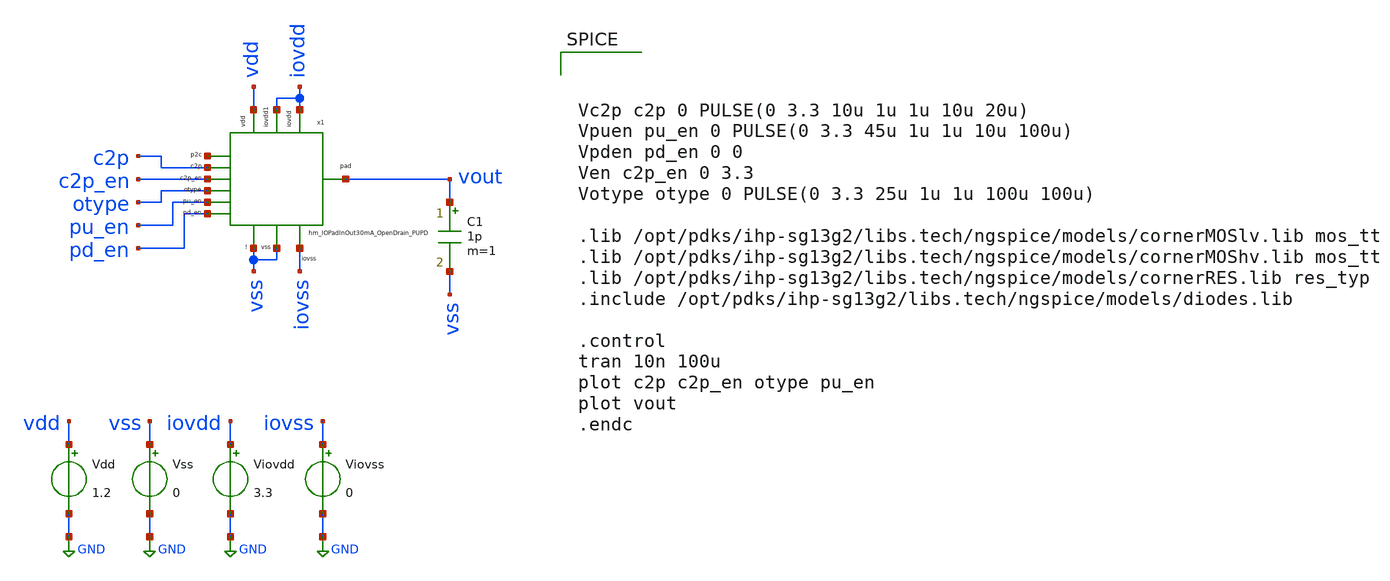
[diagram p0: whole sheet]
** sch_path: libs.tech/xschem/tests/test_hm_IOPadInOut30mA_OpenDrain_PUPD.sch
**.subckt test_hm_IOPadInOut30mA_OpenDrain_PUPD
Vdd vdd GND 1.2
Vss vss GND 0
Viovdd iovdd GND 3.3
Viovss iovss GND 0
x1 iovdd iovdd vdd pu_en c2p vout c2p_en pd_en otype net1 vss vss iovss
+ hm_IOPadInOut30mA_OpenDrain_PUPD
C1 vout vss 1p m=1
**** begin user architecture code



Vc2p c2p 0 PULSE(0 3.3 10u 1u 1u 10u 20u)
Vpuen pu_en 0 PULSE(0 3.3 45u 1u 1u 10u 100u)
Vpden pd_en 0 0
Ven c2p_en 0 3.3
Votype otype 0 PULSE(0 3.3 25u 1u 1u 100u 100u)

.lib /opt/pdks/ihp-sg13g2/libs.tech/ngspice/models/cornerMOSlv.lib mos_tt
.lib /opt/pdks/ihp-sg13g2/libs.tech/ngspice/models/cornerMOShv.lib mos_tt
.lib /opt/pdks/ihp-sg13g2/libs.tech/ngspice/models/cornerRES.lib res_typ
.include /opt/pdks/ihp-sg13g2/libs.tech/ngspice/models/diodes.lib

.control
tran 10n 100u
plot c2p c2p_en otype pu_en
plot vout
.endc



**** end user architecture code
**.ends
.GLOBAL GND
.end
